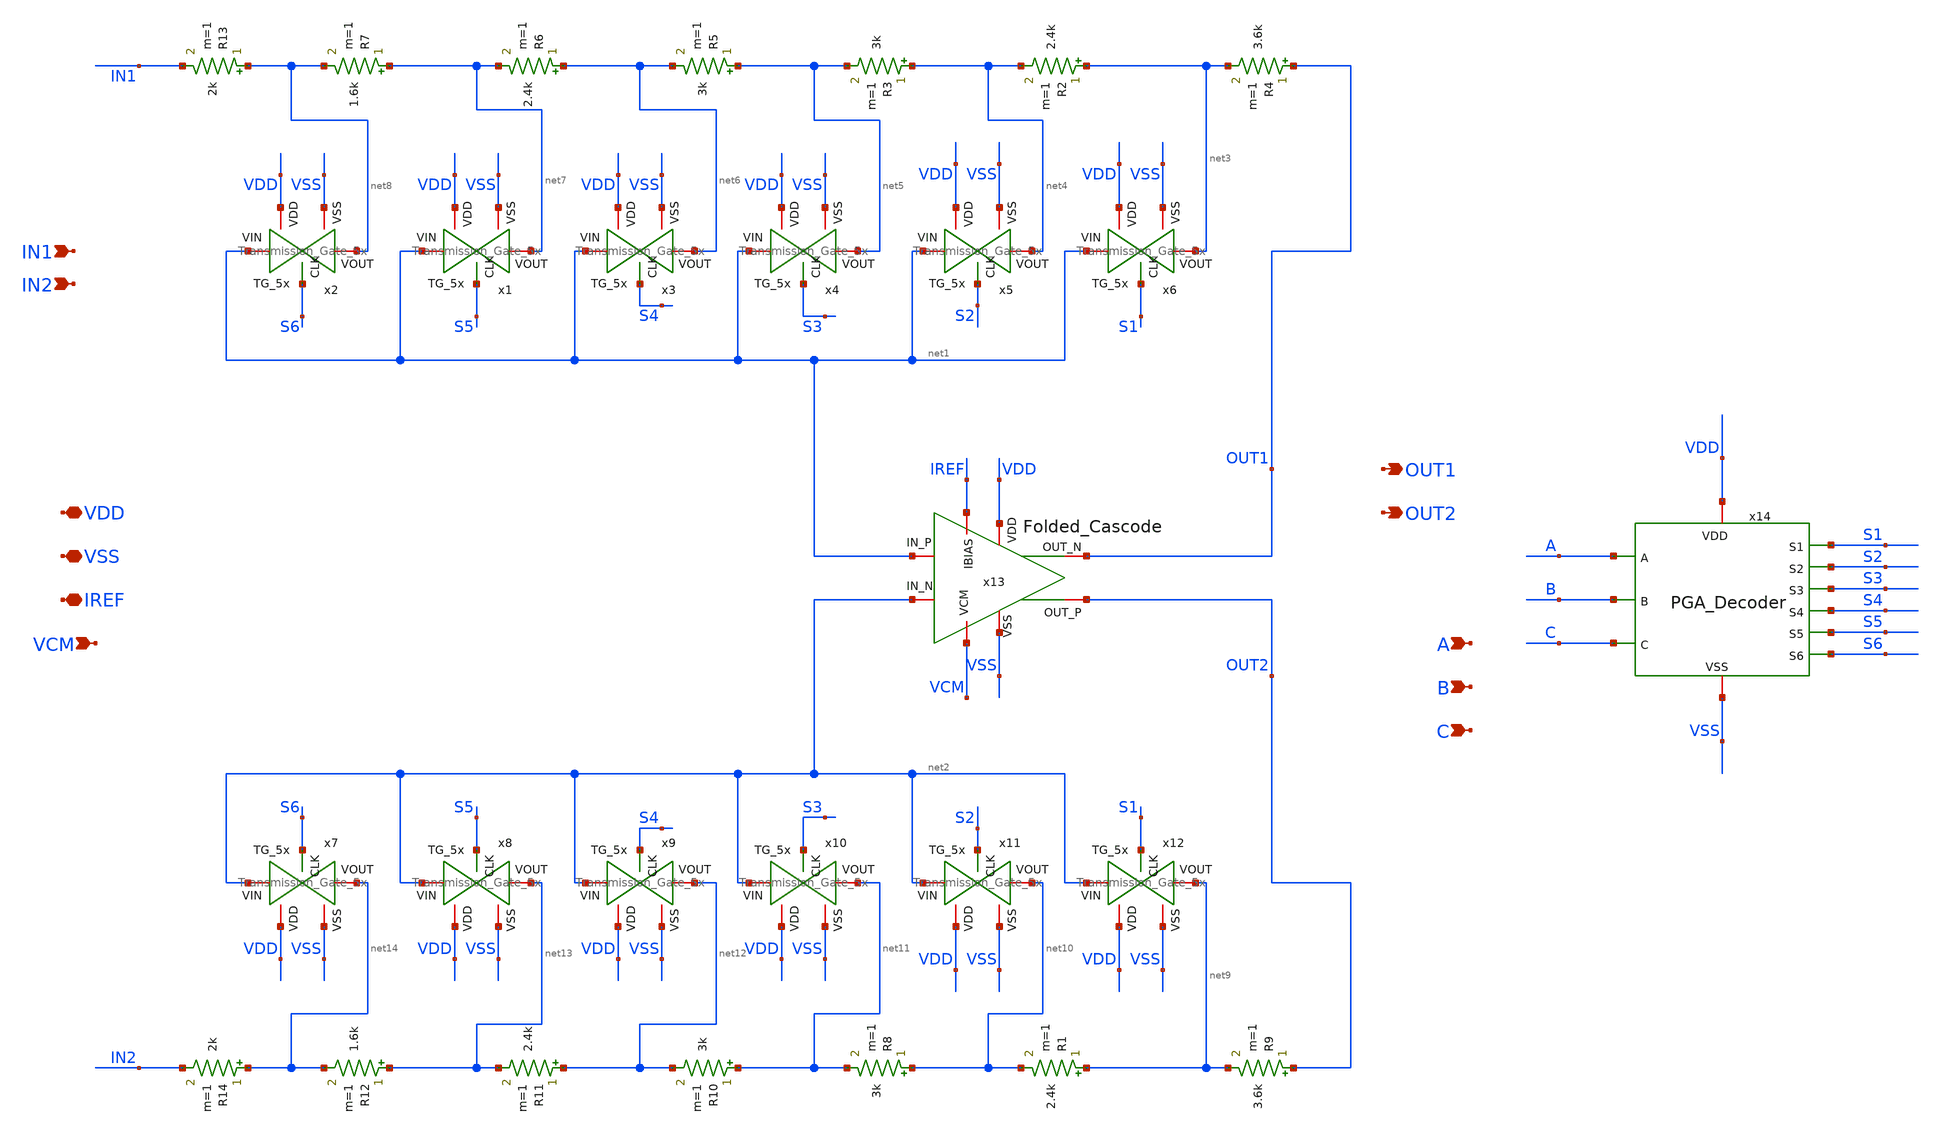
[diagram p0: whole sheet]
** sch_path: SCOP_INPUT_AND_MUX_PAKISTAN_03/Xschem/PGA_Block/PGA_block.sch
**.subckt PGA_block A B C VDD VSS IREF VCM OUT1 OUT2 IN1 IN2
*.ipin A
*.ipin B
*.ipin C
*.iopin VDD
*.iopin VSS
*.iopin IREF
*.ipin VCM
*.opin OUT1
*.opin OUT2
*.ipin IN1
*.ipin IN2
R2 net3 net4 2.4k m=1
R3 net4 net5 3k m=1
R4 OUT1 net3 3.6k m=1
R5 net5 net6 3k m=1
R6 net6 net7 2.4k m=1
R7 net7 net8 1.6k m=1
R13 net8 IN1 2k m=1
R1 net9 net10 2.4k m=1
R8 net10 net11 3k m=1
R9 OUT2 net9 3.6k m=1
R10 net11 net12 3k m=1
R11 net12 net13 2.4k m=1
R12 net13 net14 1.6k m=1
R14 net14 IN2 2k m=1
x1 VDD VSS S5 net7 net1 Transmission_Gate_5x
x2 VDD VSS S6 net8 net1 Transmission_Gate_5x
x3 VDD VSS S4 net6 net1 Transmission_Gate_5x
x4 VDD VSS S3 net5 net1 Transmission_Gate_5x
x5 VDD VSS S2 net4 net1 Transmission_Gate_5x
x6 VDD VSS S1 net3 net1 Transmission_Gate_5x
x7 VDD VSS S6 net14 net2 Transmission_Gate_5x
x8 VDD VSS S5 net13 net2 Transmission_Gate_5x
x9 VDD VSS S4 net12 net2 Transmission_Gate_5x
x10 VDD VSS S3 net11 net2 Transmission_Gate_5x
x11 VDD VSS S2 net10 net2 Transmission_Gate_5x
x12 VDD VSS S1 net9 net2 Transmission_Gate_5x
x13 VDD VSS VCM net2 net1 OUT1 OUT2 IREF Folded_Cascode
x14 S2 S3 S1 VDD A S6 B S4 C VSS S5 PGA_Decoder
**.ends
.end
